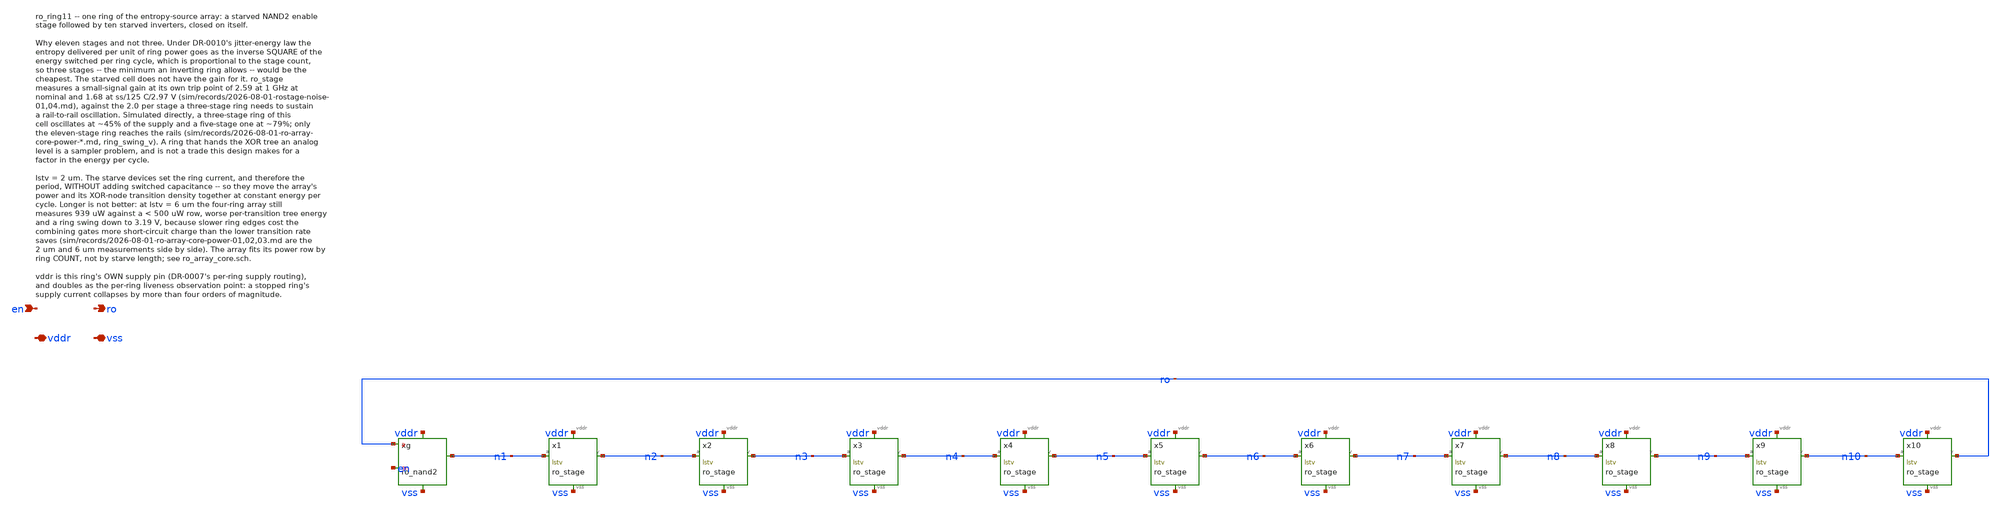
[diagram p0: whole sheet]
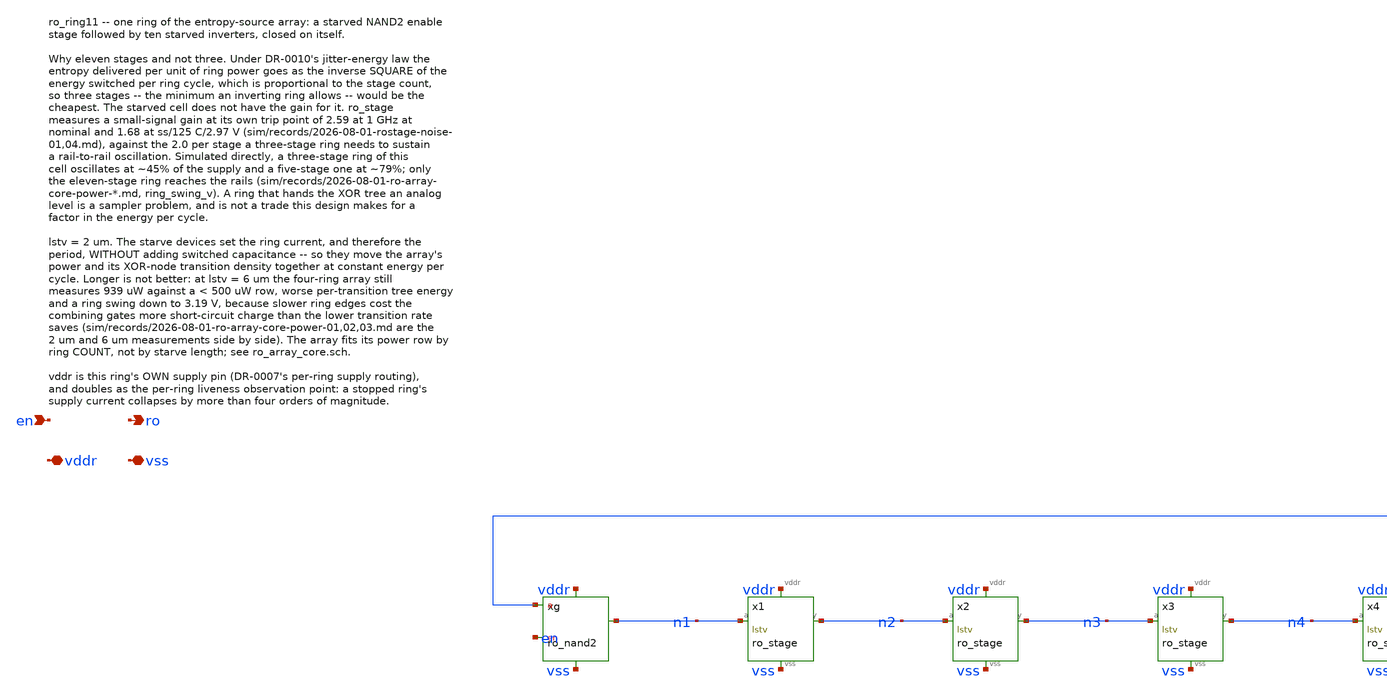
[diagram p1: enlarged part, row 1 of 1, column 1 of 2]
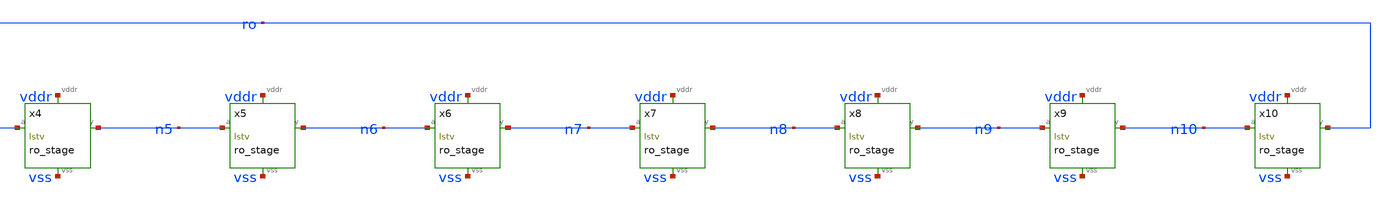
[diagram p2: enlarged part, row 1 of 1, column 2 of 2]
** sch_path: design/xschem/ro_ring11.sch
**.subckt ro_ring11 en ro vddr vss
*.ipin en
*.opin ro
*.iopin vddr
*.iopin vss
xg ro en n1 vddr vss ro_nand2 wstv=wstv lstv=lstv cld=cld
x1 n1 n2 vddr vss ro_stage wstv=wstv lstv=lstv cld=cld
x2 n2 n3 vddr vss ro_stage wstv=wstv lstv=lstv cld=cld
x3 n3 n4 vddr vss ro_stage wstv=wstv lstv=lstv cld=cld
x4 n4 n5 vddr vss ro_stage wstv=wstv lstv=lstv cld=cld
x5 n5 n6 vddr vss ro_stage wstv=wstv lstv=lstv cld=cld
x6 n6 n7 vddr vss ro_stage wstv=wstv lstv=lstv cld=cld
x7 n7 n8 vddr vss ro_stage wstv=wstv lstv=lstv cld=cld
x8 n8 n9 vddr vss ro_stage wstv=wstv lstv=lstv cld=cld
x9 n9 n10 vddr vss ro_stage wstv=wstv lstv=lstv cld=cld
x10 n10 ro vddr vss ro_stage wstv=wstv lstv=lstv cld=cld
**.ends

* expanding   symbol:  ro_nand2.sym # of pins=5
** sym_path: design/xschem/ro_nand2.sym
** sch_path: design/xschem/ro_nand2.sch
.subckt ro_nand2 a en y vddr vss  wstv=0.22u lstv=2u cld=0.5f
*.ipin a
*.ipin en
*.opin y
*.iopin vddr
*.iopin vss
XMph py vss vddr vddr pfet_03v3 L=lstv W=wstv nf=1 ad='int((nf+1)/2) * W/nf * 0.18u' as='int((nf+2)/2) * W/nf * 0.18u'
+ pd='2*int((nf+1)/2) * (W/nf + 0.18u)' ps='2*int((nf+2)/2) * (W/nf + 0.18u)' nrd='0.18u / W' nrs='0.18u / W'
+ sa=0 sb=0 sd=0 m=1
XMpa y a py vddr pfet_03v3 L=0.28u W=0.44u nf=1 ad='int((nf+1)/2) * W/nf * 0.18u' as='int((nf+2)/2) * W/nf * 0.18u'
+ pd='2*int((nf+1)/2) * (W/nf + 0.18u)' ps='2*int((nf+2)/2) * (W/nf + 0.18u)' nrd='0.18u / W' nrs='0.18u / W'
+ sa=0 sb=0 sd=0 m=1
XMpb y en py vddr pfet_03v3 L=0.28u W=0.44u nf=1 ad='int((nf+1)/2) * W/nf * 0.18u' as='int((nf+2)/2) * W/nf * 0.18u'
+ pd='2*int((nf+1)/2) * (W/nf + 0.18u)' ps='2*int((nf+2)/2) * (W/nf + 0.18u)' nrd='0.18u / W' nrs='0.18u / W'
+ sa=0 sb=0 sd=0 m=1
XMna y a nm vss nfet_03v3 L=0.28u W=0.44u nf=1 ad='int((nf+1)/2) * W/nf * 0.18u' as='int((nf+2)/2) * W/nf * 0.18u'
+ pd='2*int((nf+1)/2) * (W/nf + 0.18u)' ps='2*int((nf+2)/2) * (W/nf + 0.18u)' nrd='0.18u / W' nrs='0.18u / W'
+ sa=0 sb=0 sd=0 m=1
XMnb nm en ny vss nfet_03v3 L=0.28u W=0.44u nf=1 ad='int((nf+1)/2) * W/nf * 0.18u' as='int((nf+2)/2) * W/nf * 0.18u'
+ pd='2*int((nf+1)/2) * (W/nf + 0.18u)' ps='2*int((nf+2)/2) * (W/nf + 0.18u)' nrd='0.18u / W' nrs='0.18u / W'
+ sa=0 sb=0 sd=0 m=1
XMnt ny vddr vss vss nfet_03v3 L=lstv W=wstv nf=1 ad='int((nf+1)/2) * W/nf * 0.18u' as='int((nf+2)/2) * W/nf * 0.18u'
+ pd='2*int((nf+1)/2) * (W/nf + 0.18u)' ps='2*int((nf+2)/2) * (W/nf + 0.18u)' nrd='0.18u / W' nrs='0.18u / W'
+ sa=0 sb=0 sd=0 m=1
Cld y vss 'cld' m=1
.ends


* expanding   symbol:  ro_stage.sym # of pins=4
** sym_path: design/xschem/ro_stage.sym
** sch_path: design/xschem/ro_stage.sch
.subckt ro_stage a y vddr vss  wstv=0.22u lstv=2u cld=0.5f
*.ipin a
*.opin y
*.iopin vddr
*.iopin vss
XMph py vss vddr vddr pfet_03v3 L=lstv W=wstv nf=1 ad='int((nf+1)/2) * W/nf * 0.18u' as='int((nf+2)/2) * W/nf * 0.18u'
+ pd='2*int((nf+1)/2) * (W/nf + 0.18u)' ps='2*int((nf+2)/2) * (W/nf + 0.18u)' nrd='0.18u / W' nrs='0.18u / W'
+ sa=0 sb=0 sd=0 m=1
XMp y a py vddr pfet_03v3 L=0.28u W=0.44u nf=1 ad='int((nf+1)/2) * W/nf * 0.18u' as='int((nf+2)/2) * W/nf * 0.18u'
+ pd='2*int((nf+1)/2) * (W/nf + 0.18u)' ps='2*int((nf+2)/2) * (W/nf + 0.18u)' nrd='0.18u / W' nrs='0.18u / W'
+ sa=0 sb=0 sd=0 m=1
XMn y a ny vss nfet_03v3 L=0.28u W=0.22u nf=1 ad='int((nf+1)/2) * W/nf * 0.18u' as='int((nf+2)/2) * W/nf * 0.18u'
+ pd='2*int((nf+1)/2) * (W/nf + 0.18u)' ps='2*int((nf+2)/2) * (W/nf + 0.18u)' nrd='0.18u / W' nrs='0.18u / W'
+ sa=0 sb=0 sd=0 m=1
XMnt ny vddr vss vss nfet_03v3 L=lstv W=wstv nf=1 ad='int((nf+1)/2) * W/nf * 0.18u' as='int((nf+2)/2) * W/nf * 0.18u'
+ pd='2*int((nf+1)/2) * (W/nf + 0.18u)' ps='2*int((nf+2)/2) * (W/nf + 0.18u)' nrd='0.18u / W' nrs='0.18u / W'
+ sa=0 sb=0 sd=0 m=1
Cld y vss 'cld' m=1
.ends

.end
